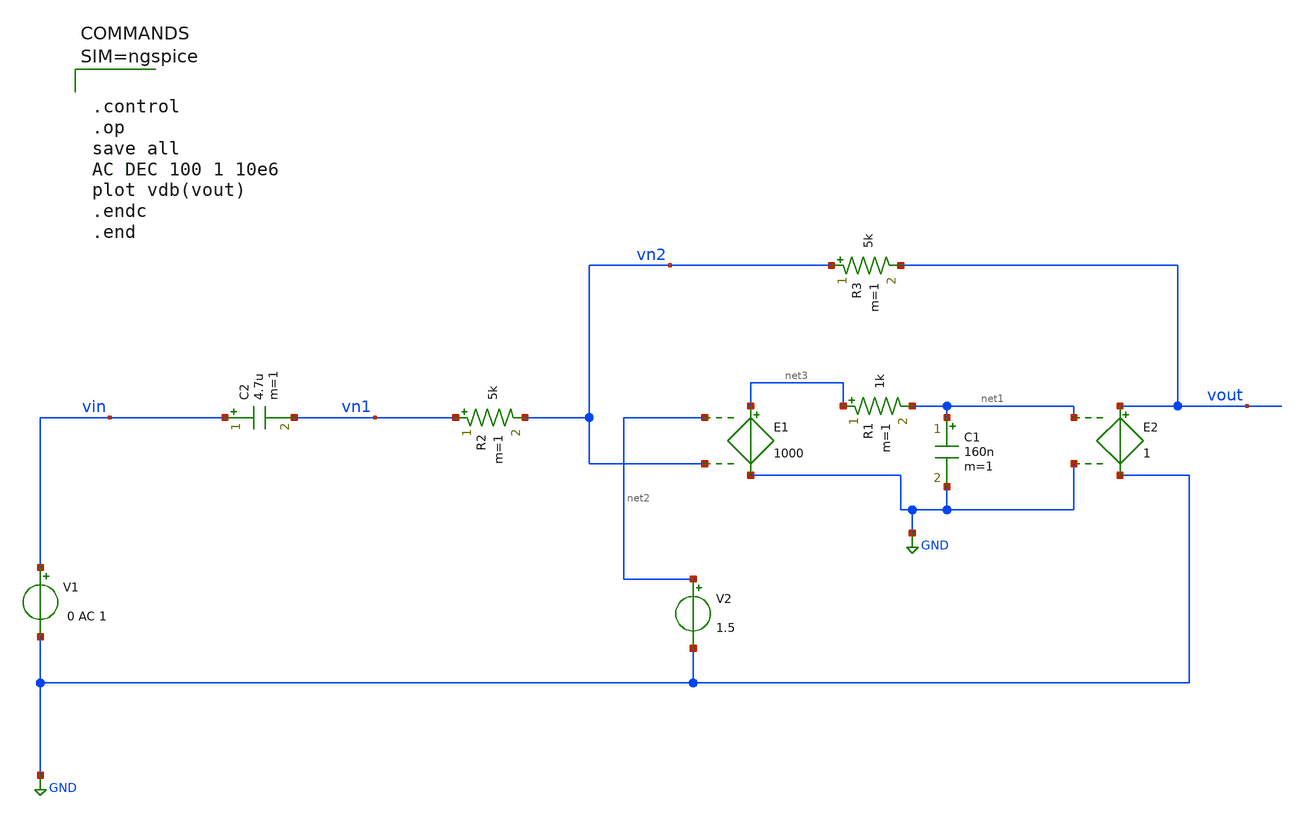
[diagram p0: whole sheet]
** sch_path: xschem/oplow.sch
**.subckt oplow
E1 net3 GND net2 vn2 1000
E2 vout GND net1 GND 1
R1 net3 net1 1k m=1
C1 net1 GND 160n m=1
R2 vn1 vn2 5k m=1
R3 vn2 vout 5k m=1
C2 vin vn1 4.7u m=1
V1 vin GND 0 AC 1
V2 net2 GND 1.5
**** begin user architecture code



.control
.op
save all
AC DEC 100 1 10e6
plot vdb(vout)
.endc
.end



**** end user architecture code
**.ends
.GLOBAL GND
.end
